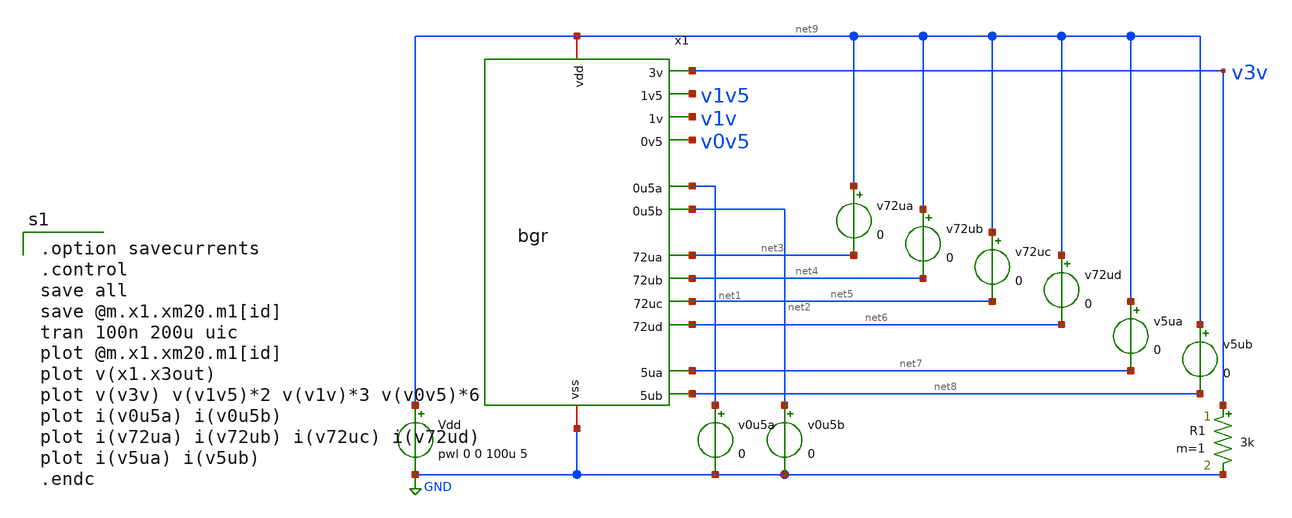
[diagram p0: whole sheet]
** sch_path: member_project/DCDC/ShuntaroOHNO/xschem/bgr_tran.sch
**.subckt bgr_tran
Vdd net9 GND pwl 0 0 100u 5
x1 net9 v3v net2 net1 v1v5 net8 net7 net5 net4 net3 v1v v0v5 GND net6 bgr
v0u5a net1 GND 0
v0u5b net2 GND 0
v72ua net9 net3 0
v72ub net9 net4 0
v72uc net9 net5 0
v72ud net9 net6 0
v5ua net9 net7 0
v5ub net9 net8 0
R1 v3v GND 3k m=1
**** begin user architecture code
 .include $::LIB/ip62_models

.option savecurrents
.control
save all
save @m.x1.xm20.m1[id]
tran 100n 200u uic
plot @m.x1.xm20.m1[id]
plot v(x1.x3out)
plot v(v3v) v(v1v5)*2 v(v1v)*3 v(v0v5)*6
plot i(v0u5a) i(v0u5b)
plot i(v72ua) i(v72ub) i(v72uc) i(v72ud)
plot i(v5ua) i(v5ub)
.endc

**** end user architecture code
**.ends
.GLOBAL GND
.end
